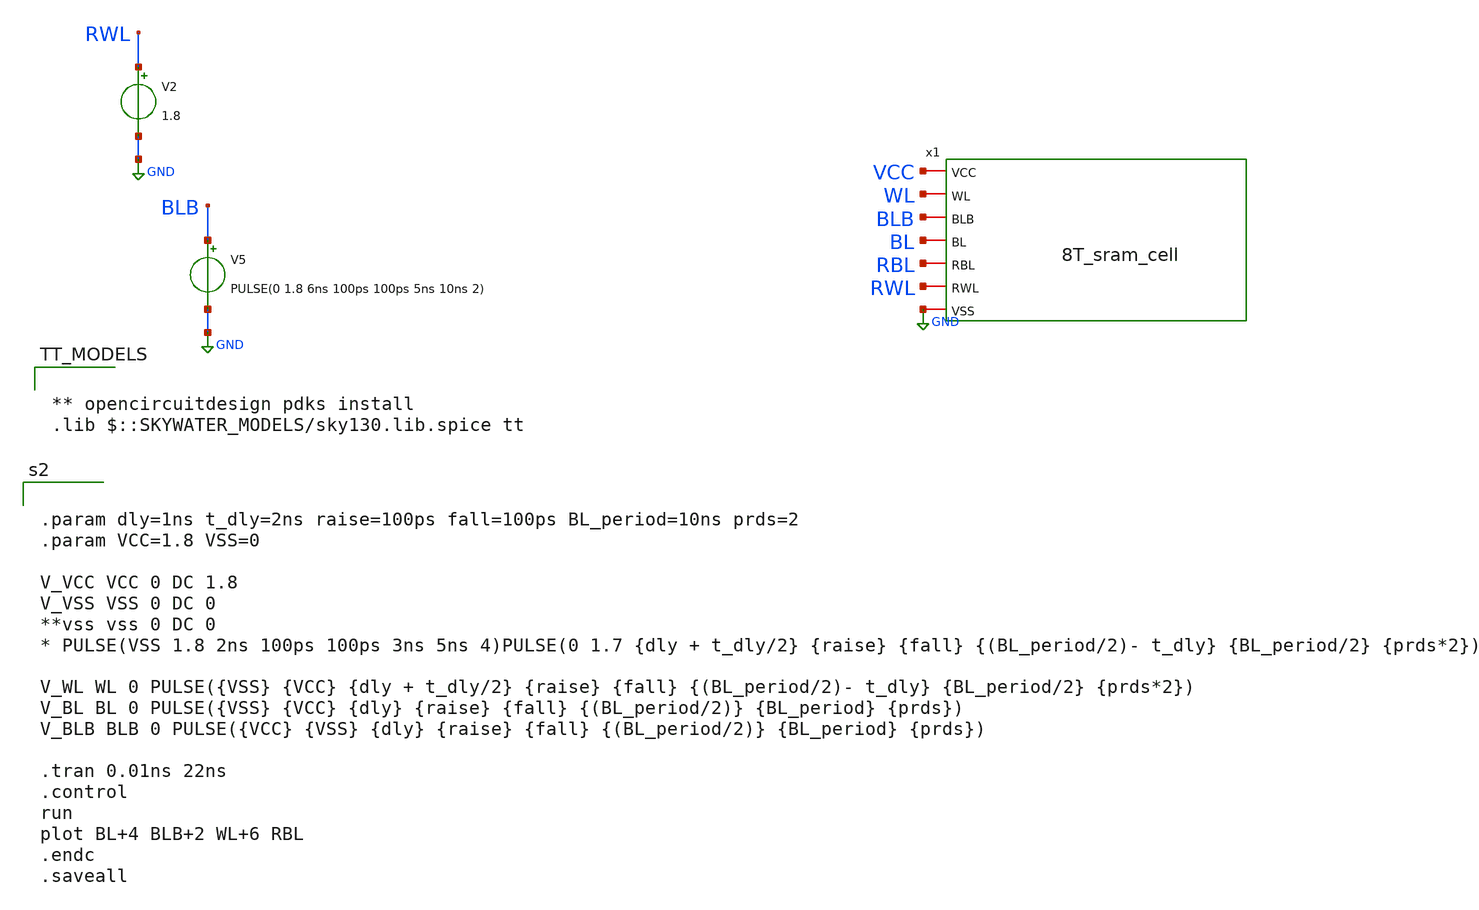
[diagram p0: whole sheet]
** sch_path: 8T_sram_mac.sch
**.subckt 8T_sram_mac
V2 RWL GND 1.8
V5 BLB GND PULSE(0 1.8 6ns 100ps 100ps 5ns 10ns 2)
x1 VCC WL BLB BL RBL RWL GND 8T_sram_cell
**** begin user architecture code


.param dly=1ns t_dly=2ns raise=100ps fall=100ps BL_period=10ns prds=2
.param VCC=1.8 VSS=0

V_VCC VCC 0 DC 1.8
V_VSS VSS 0 DC 0
**vss vss 0 DC 0
* PULSE(VSS 1.8 2ns 100ps 100ps 3ns 5ns 4)PULSE(0 1.7 {dly + t_dly/2} {raise} {fall} {(BL_period/2)- t_dly}
*+ {BL_period/2} {prds*2})

V_WL WL 0 PULSE({VSS} {VCC} {dly + t_dly/2} {raise} {fall} {(BL_period/2)- t_dly} {BL_period/2} {prds*2})
V_BL BL 0 PULSE({VSS} {VCC} {dly} {raise} {fall} {(BL_period/2)} {BL_period} {prds})
V_BLB BLB 0 PULSE({VCC} {VSS} {dly} {raise} {fall} {(BL_period/2)} {BL_period} {prds})

.tran 0.01ns 22ns
.control
run
plot BL+4 BLB+2 WL+6 RBL
.endc
.saveall




** opencircuitdesign pdks install
.lib $::SKYWATER_MODELS/sky130.lib.spice tt

**** end user architecture code
**.ends

* expanding   symbol:  8T_sram_cell.sym # of pins=7
** sym_path: 8T_sram_cell.sym
** sch_path: 8T_sram_cell.sch
.subckt 8T_sram_cell VCC WL BLB BL RBL RWL VSS
*.iopin VCC
*.iopin BLB
*.iopin WL
*.iopin BL
*.iopin VSS
*.iopin RBL
*.iopin RWL
XM1 q_bar q VSS VSS sky130_fd_pr__nfet_01v8 L=0.15 W=1 nf=1 ad='int((1 + 1)/2) * 1 / 1 * 0.29' as='int((1 + 2)/2) * 1 / 1 * 0.29'
+ pd='2*int((1 + 1)/2) * (1 / 1 + 0.29)' ps='2*int((1 + 2)/2) * (1 / 1 + 0.29)' nrd='0.29 / 1 ' nrs='0.29 / 1 '
+ sa=0 sb=0 sd=0 mult=1 m=1
XM2 q q_bar VSS VSS sky130_fd_pr__nfet_01v8 L=0.15 W=1 nf=1 ad='int((1 + 1)/2) * 1 / 1 * 0.29' as='int((1 + 2)/2) * 1 / 1 * 0.29'
+ pd='2*int((1 + 1)/2) * (1 / 1 + 0.29)' ps='2*int((1 + 2)/2) * (1 / 1 + 0.29)' nrd='0.29 / 1 ' nrs='0.29 / 1 '
+ sa=0 sb=0 sd=0 mult=1 m=1
XM3 q_bar q VCC VCC sky130_fd_pr__pfet_01v8 L=0.15 W=4 nf=1 ad='int((1 + 1)/2) * 4 / 1 * 0.29' as='int((1 + 2)/2) * 4 / 1 * 0.29'
+ pd='2*int((1 + 1)/2) * (4 / 1 + 0.29)' ps='2*int((1 + 2)/2) * (4 / 1 + 0.29)' nrd='0.29 / 4 ' nrs='0.29 / 4 '
+ sa=0 sb=0 sd=0 mult=1 m=1
XM4 q q_bar VCC VCC sky130_fd_pr__pfet_01v8 L=0.15 W=4 nf=1 ad='int((1 + 1)/2) * 4 / 1 * 0.29' as='int((1 + 2)/2) * 4 / 1 * 0.29'
+ pd='2*int((1 + 1)/2) * (4 / 1 + 0.29)' ps='2*int((1 + 2)/2) * (4 / 1 + 0.29)' nrd='0.29 / 4 ' nrs='0.29 / 4 '
+ sa=0 sb=0 sd=0 mult=1 m=1
XM5 BLB WL q_bar VSS sky130_fd_pr__nfet_01v8 L=0.15 W=1 nf=1 ad='int((1 + 1)/2) * 1 / 1 * 0.29' as='int((1 + 2)/2) * 1 / 1 * 0.29'
+ pd='2*int((1 + 1)/2) * (1 / 1 + 0.29)' ps='2*int((1 + 2)/2) * (1 / 1 + 0.29)' nrd='0.29 / 1 ' nrs='0.29 / 1 '
+ sa=0 sb=0 sd=0 mult=1 m=1
XM8 q WL BL VSS sky130_fd_pr__nfet_01v8 L=0.15 W=1 nf=1 ad='int((1 + 1)/2) * 1 / 1 * 0.29' as='int((1 + 2)/2) * 1 / 1 * 0.29'
+ pd='2*int((1 + 1)/2) * (1 / 1 + 0.29)' ps='2*int((1 + 2)/2) * (1 / 1 + 0.29)' nrd='0.29 / 1 ' nrs='0.29 / 1 '
+ sa=0 sb=0 sd=0 mult=1 m=1
XM6 net1 q_bar VSS VSS sky130_fd_pr__nfet_01v8 L=0.15 W=1 nf=1 ad='int((1 + 1)/2) * 1 / 1 * 0.29' as='int((1 + 2)/2) * 1 / 1 * 0.29'
+ pd='2*int((1 + 1)/2) * (1 / 1 + 0.29)' ps='2*int((1 + 2)/2) * (1 / 1 + 0.29)' nrd='0.29 / 1 ' nrs='0.29 / 1 '
+ sa=0 sb=0 sd=0 mult=1 m=1
XM7 RBL RWL net1 VSS sky130_fd_pr__nfet_01v8 L=0.15 W=1 nf=1 ad='int((1 + 1)/2) * 1 / 1 * 0.29' as='int((1 + 2)/2) * 1 / 1 * 0.29'
+ pd='2*int((1 + 1)/2) * (1 / 1 + 0.29)' ps='2*int((1 + 2)/2) * (1 / 1 + 0.29)' nrd='0.29 / 1 ' nrs='0.29 / 1 '
+ sa=0 sb=0 sd=0 mult=1 m=1
.ends

.GLOBAL GND
.end
